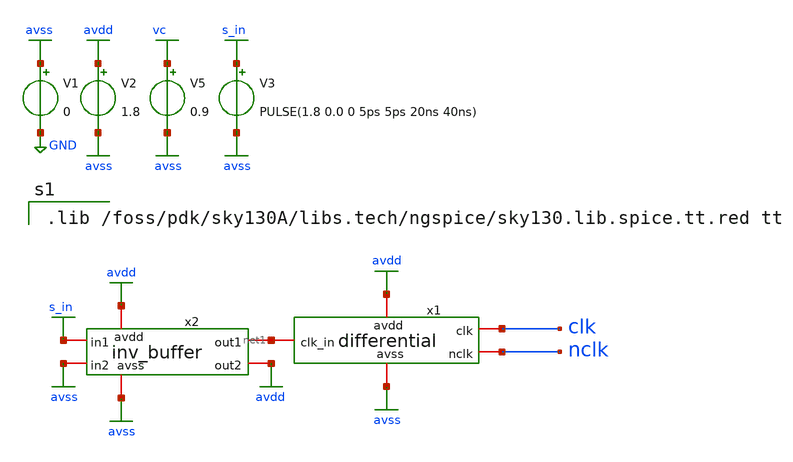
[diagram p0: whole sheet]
** sch_path: xschem/differential_sim1.sch
**.subckt differential_sim1
V1 avss GND 0
V2 avdd avss 1.8
V3 s_in avss PULSE(1.8 0.0 0 5ps 5ps 20ns 40ns)
V5 vc avss 0.9
x1 avdd avss net1 clk nclk differential
x2 avdd avss net1 avdd avss s_in inv_buffer
**** begin user architecture code

.lib /foss/pdk/sky130A/libs.tech/ngspice/sky130.lib.spice.tt.red tt



.control
save s_in clk nclk @V1[i] @V3[i]
tran 0.01n 120n 0n
plot s_in clk nclk
*plot clk
*plot nclk
plot @V1[i] @V3[i]
.endc
.end


**** end user architecture code
**.ends
.GLOBAL avdd
.GLOBAL avss
.GLOBAL GND
.GLOBAL vc
.GLOBAL s_in
.end
